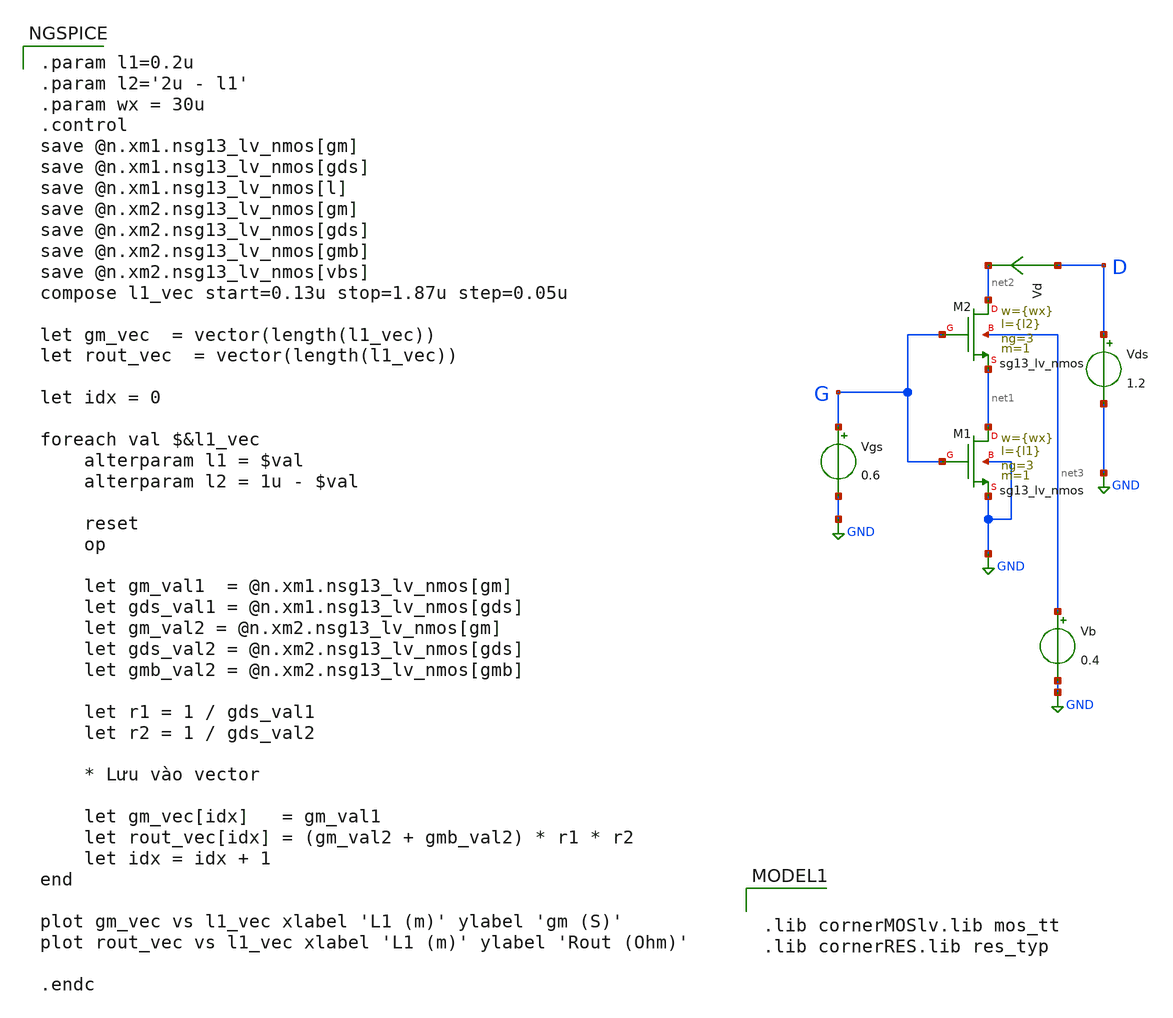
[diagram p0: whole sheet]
** sch_path: xschem/self-cascode-nmos.sch
**.subckt self-cascode-nmos
Vgs G GND 0.6
Vds D GND 1.2
Vd D net2 0
.save i(vd)
XM1 net1 G GND GND sg13_lv_nmos w={wx} l={l1} ng=3 m=1 mm_ok=1
XM2 net2 G net1 net3 sg13_lv_nmos w={wx} l={l2} ng=3 m=1 mm_ok=1
Vb net3 GND 0.4
**** begin user architecture code

.lib cornerMOSlv.lib mos_tt
.lib cornerRES.lib res_typ


.param l1=0.2u
.param l2='2u - l1'
.param wx = 30u
.control
save @n.xm1.nsg13_lv_nmos[gm]
save @n.xm1.nsg13_lv_nmos[gds]
save @n.xm1.nsg13_lv_nmos[l]
save @n.xm2.nsg13_lv_nmos[gm]
save @n.xm2.nsg13_lv_nmos[gds]
save @n.xm2.nsg13_lv_nmos[gmb]
save @n.xm2.nsg13_lv_nmos[vbs]
compose l1_vec start=0.13u stop=1.87u step=0.05u

let gm_vec  = vector(length(l1_vec))
let rout_vec  = vector(length(l1_vec))

let idx = 0

foreach val $&l1_vec
    alterparam l1 = $val
    alterparam l2 = 1u - $val

    reset
    op

    let gm_val1  = @n.xm1.nsg13_lv_nmos[gm]
    let gds_val1 = @n.xm1.nsg13_lv_nmos[gds]
    let gm_val2 = @n.xm2.nsg13_lv_nmos[gm]
    let gds_val2 = @n.xm2.nsg13_lv_nmos[gds]
    let gmb_val2 = @n.xm2.nsg13_lv_nmos[gmb]

    let r1 = 1 / gds_val1
    let r2 = 1 / gds_val2

    * Lưu vào vector

    let gm_vec[idx]   = gm_val1
    let rout_vec[idx] = (gm_val2 + gmb_val2) * r1 * r2
    let idx = idx + 1
end

plot gm_vec vs l1_vec xlabel 'L1 (m)' ylabel 'gm (S)'
plot rout_vec vs l1_vec xlabel 'L1 (m)' ylabel 'Rout (Ohm)'

.endc


**** end user architecture code
**.ends
.GLOBAL GND
.end
